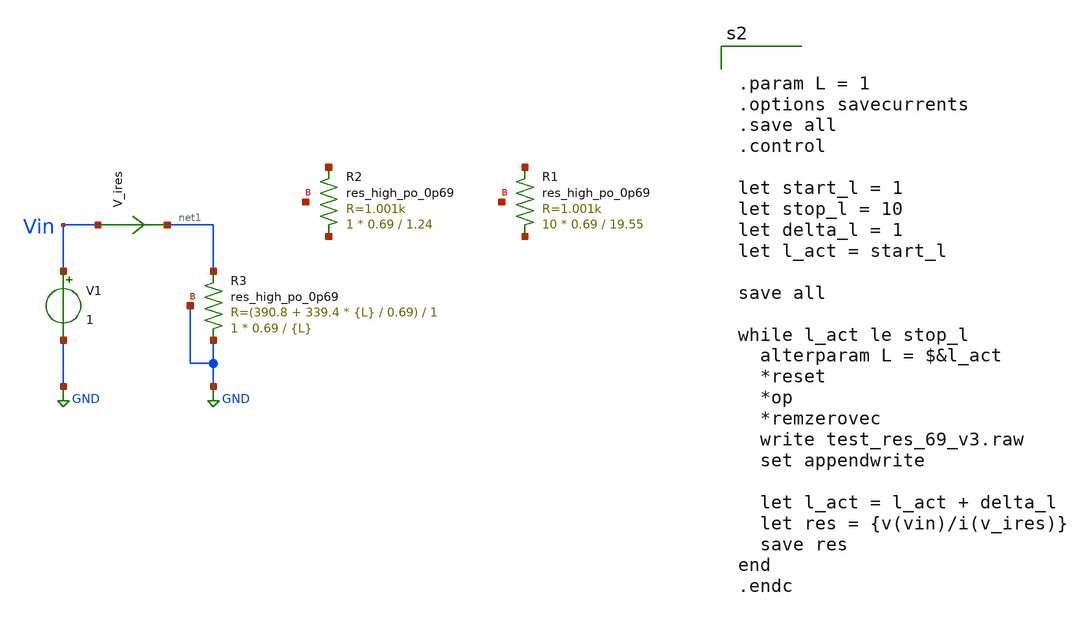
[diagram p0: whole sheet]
** sch_path: xschem/test_res_69_v3.sch
**.subckt test_res_69_v3
V1 Vin GND 1
V_ires Vin net1 0
.save i(v_ires)
XR1 net2 net3 net4 sky130_fd_pr__res_high_po_0p69 L=19.55 mult=10 m=10
XR2 net5 net6 net7 sky130_fd_pr__res_high_po_0p69 L=1.24 mult=1 m=1
XR3 GND net1 GND sky130_fd_pr__res_high_po_0p69 L={L} mult=1 m=1
**** begin user architecture code


.param L = 1
.options savecurrents
.save all
.control

let start_l = 1
let stop_l = 10
let delta_l = 1
let l_act = start_l

save all

while l_act le stop_l
  alterparam L = $&l_act
  *reset
  *op
  *remzerovec
  write test_res_69_v3.raw
  set appendwrite

  let l_act = l_act + delta_l
  let res = {v(vin)/i(v_ires)}
  save res
end
.endc


** opencircuitdesign pdks install
.lib $::SKYWATER_MODELS/sky130.lib.spice tt


**** end user architecture code
**.ends
.GLOBAL GND
.end
